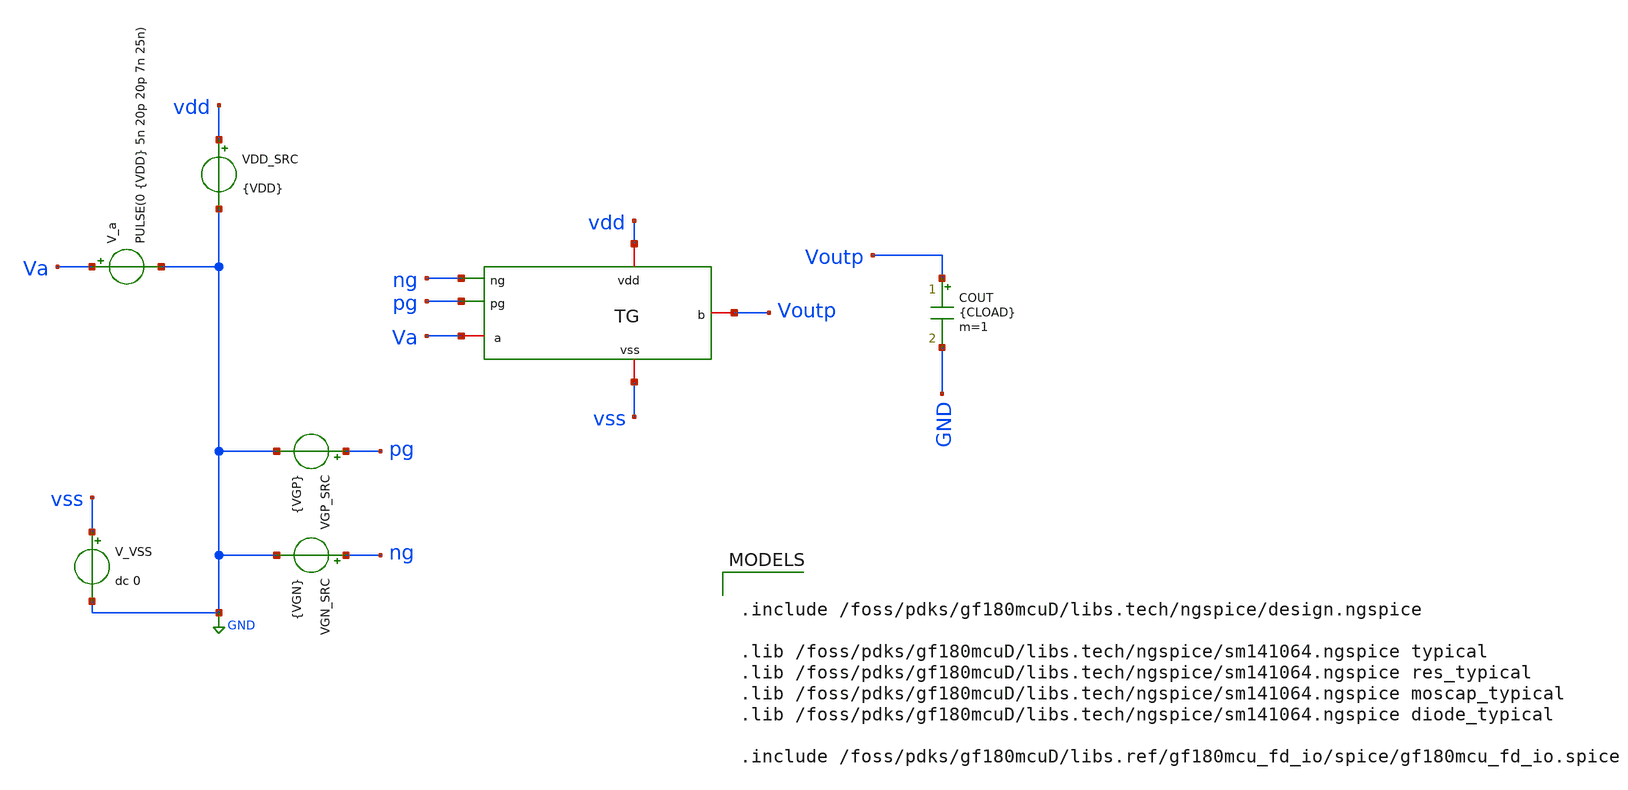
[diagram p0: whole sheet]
** sch_path: xschem/SAR_ADC/tb/tg_tb.sch
**.subckt tg_tb
VGN_SRC ng GND {VGN}
VDD_SRC vdd GND {VDD}
VGP_SRC pg GND {VGP}
x1 vss ng pg vdd Va Voutp tg
V_a Va GND PULSE(0 {VDD} 5n 20p 20p 7n 25n)
V_VSS vss GND dc 0
COUT Voutp GND {CLOAD} m=1
**** begin user architecture code



.param VDD=3.3
.param VGN=3.3
.param VGP=0


.param N_WU=8u
.param P_WU=12u
.param N_L=0.5u
.param P_L=0.5u
.param N_NF=1
.param P_NF=1
.param nf=1

.param N_M=4
.param P_M=8

.param Cu=5f
.param CLOAD=5.12p

.options savecurrents
.options reltol=1e-4 abstol=1e-12 vntol=1e-6 method=gear

.save v(Va) v(Voutp) v(ng) v(pg) i(VDD_SRC)

.control

shell rm -f tg_final_bidirectional_results.txt
shell rm -f tg_final_candidates.txt

echo ================================================== > tg_final_bidirectional_results.txt
echo GF180MCU TG final bidirectional sizing sweep >> tg_final_bidirectional_results.txt
echo Purpose: SAR ADC CDAC sampling switch final sizing >> tg_final_bidirectional_results.txt
echo ================================================== >> tg_final_bidirectional_results.txt
echo VDD = 3.3 V >> tg_final_bidirectional_results.txt
echo Va source must be: PULSE(0 {VDD} 5n 20p 20p 7n 25n) >> tg_final_bidirectional_results.txt
echo Load = 5.12 pF >> tg_final_bidirectional_results.txt
echo Unit NMOS width = 8u, unit PMOS width = 12u, nf=1 >> tg_final_bidirectional_results.txt
echo Settling target = 0.5 LSB = 3.3/2048 = 1.611 mV >> tg_final_bidirectional_results.txt
echo Rising edge at 5 ns, falling edge at 12 ns >> tg_final_bidirectional_results.txt
echo . >> tg_final_bidirectional_results.txt
echo columns: N_M P_M N_Wtot_u P_Wtot_u Va_r4 Vout_r4 erise_4ns Va_f4 Vout_f4 efall_4ns pass_4ns
+ Va_r5 Vout_r5 erise_5ns Va_f5 Vout_f5 efall_5ns pass_5ns >> tg_final_bidirectional_results.txt
echo ================================================== >> tg_final_bidirectional_results.txt

echo ================================================== > tg_final_candidates.txt
echo TG final candidates passing both rising and falling at 4 ns >> tg_final_candidates.txt
echo columns: N_M P_M N_Wtot_u P_Wtot_u erise_4ns efall_4ns erise_5ns efall_5ns >>
+ tg_final_candidates.txt
echo ================================================== >> tg_final_candidates.txt

let err10 = 3.3/2048

alterparam N_WU=8u
alterparam P_WU=12u
alterparam N_L=0.5u
alterparam P_L=0.5u
alterparam N_NF=1
alterparam P_NF=1
alterparam VGN=3.3
alterparam VGP=0
alterparam VDD=3.3
alterparam CLOAD=5.12p

foreach nm 2 3 4 5 6

  foreach pm 6 7 8 9 10

    alterparam N_M=$nm
    alterparam P_M=$pm

    let nwtot_u = 8 * $nm
    let pwtot_u = 12 * $pm

    reset
    tran 2p 18n

    * Rising edge occurs at 5 ns.
    * Rising +4 ns = 9 ns.
    * Rising +5 ns = 10 ns.
    meas tran var4 FIND v(Va) AT=9n
    meas tran vor4 FIND v(Voutp) AT=9n
    meas tran var5 FIND v(Va) AT=10n
    meas tran vor5 FIND v(Voutp) AT=10n

    let er4 = abs(3.3 - vor4)
    let er5 = abs(3.3 - vor5)

    * Falling edge occurs at 12 ns.
    * Falling +4 ns = 16 ns.
    * Falling +5 ns = 17 ns.
    meas tran vaf4 FIND v(Va) AT=16n
    meas tran vof4 FIND v(Voutp) AT=16n
    meas tran vaf5 FIND v(Va) AT=17n
    meas tran vof5 FIND v(Voutp) AT=17n

    let ef4 = abs(vof4)
    let ef5 = abs(vof5)

    let pass4 = 0
    let pass5 = 0

    if er4 < err10
      if ef4 < err10
        let pass4 = 1
      end
    end

    if er5 < err10
      if ef5 < err10
        let pass5 = 1
      end
    end

    echo $nm $pm $&nwtot_u $&pwtot_u $&var4 $&vor4 $&er4 $&vaf4 $&vof4 $&ef4 $&pass4 $&var5 $&vor5
+ $&er5 $&vaf5 $&vof5 $&ef5 $&pass5 >> tg_final_bidirectional_results.txt

    if pass4 > 0.5
      echo $nm $pm $&nwtot_u $&pwtot_u $&er4 $&ef4 $&er5 $&ef5 >> tg_final_candidates.txt
    end

  end
end

echo TG final bidirectional sizing sweep complete.
.endc





.include /foss/pdks/gf180mcuD/libs.tech/ngspice/design.ngspice

.lib /foss/pdks/gf180mcuD/libs.tech/ngspice/sm141064.ngspice typical
.lib /foss/pdks/gf180mcuD/libs.tech/ngspice/sm141064.ngspice res_typical
.lib /foss/pdks/gf180mcuD/libs.tech/ngspice/sm141064.ngspice moscap_typical
.lib /foss/pdks/gf180mcuD/libs.tech/ngspice/sm141064.ngspice diode_typical

.include /foss/pdks/gf180mcuD/libs.ref/gf180mcu_fd_io/spice/gf180mcu_fd_io.spice

**** end user architecture code
**.ends

* expanding   symbol:  tg.sym # of pins=6
** sym_path: tg.sym
** sch_path: tg.sch
.subckt tg vss ng pg vdd a b
*.ipin ng
*.iopin vdd
*.ipin pg
*.iopin a
*.iopin b
*.iopin vss
XM2 b pg a vdd pfet_03v3 L=0.5u W=12u nf=1 ad='int((nf+1)/2) * W/nf * 0.18u' as='int((nf+2)/2) * W/nf * 0.18u'
+ pd='2*int((nf+1)/2) * (W/nf + 0.18u)' ps='2*int((nf+2)/2) * (W/nf + 0.18u)' nrd='0.18u / W' nrs='0.18u / W'
+ sa=0 sb=0 sd=0 m=8
XM1 b ng a vss nfet_03v3 L=0.5u W=8u nf=1 ad='int((nf+1)/2) * W/nf * 0.18u' as='int((nf+2)/2) * W/nf * 0.18u'
+ pd='2*int((nf+1)/2) * (W/nf + 0.18u)' ps='2*int((nf+2)/2) * (W/nf + 0.18u)' nrd='0.18u / W' nrs='0.18u / W'
+ sa=0 sb=0 sd=0 m=4
.ends

.GLOBAL GND
.end
